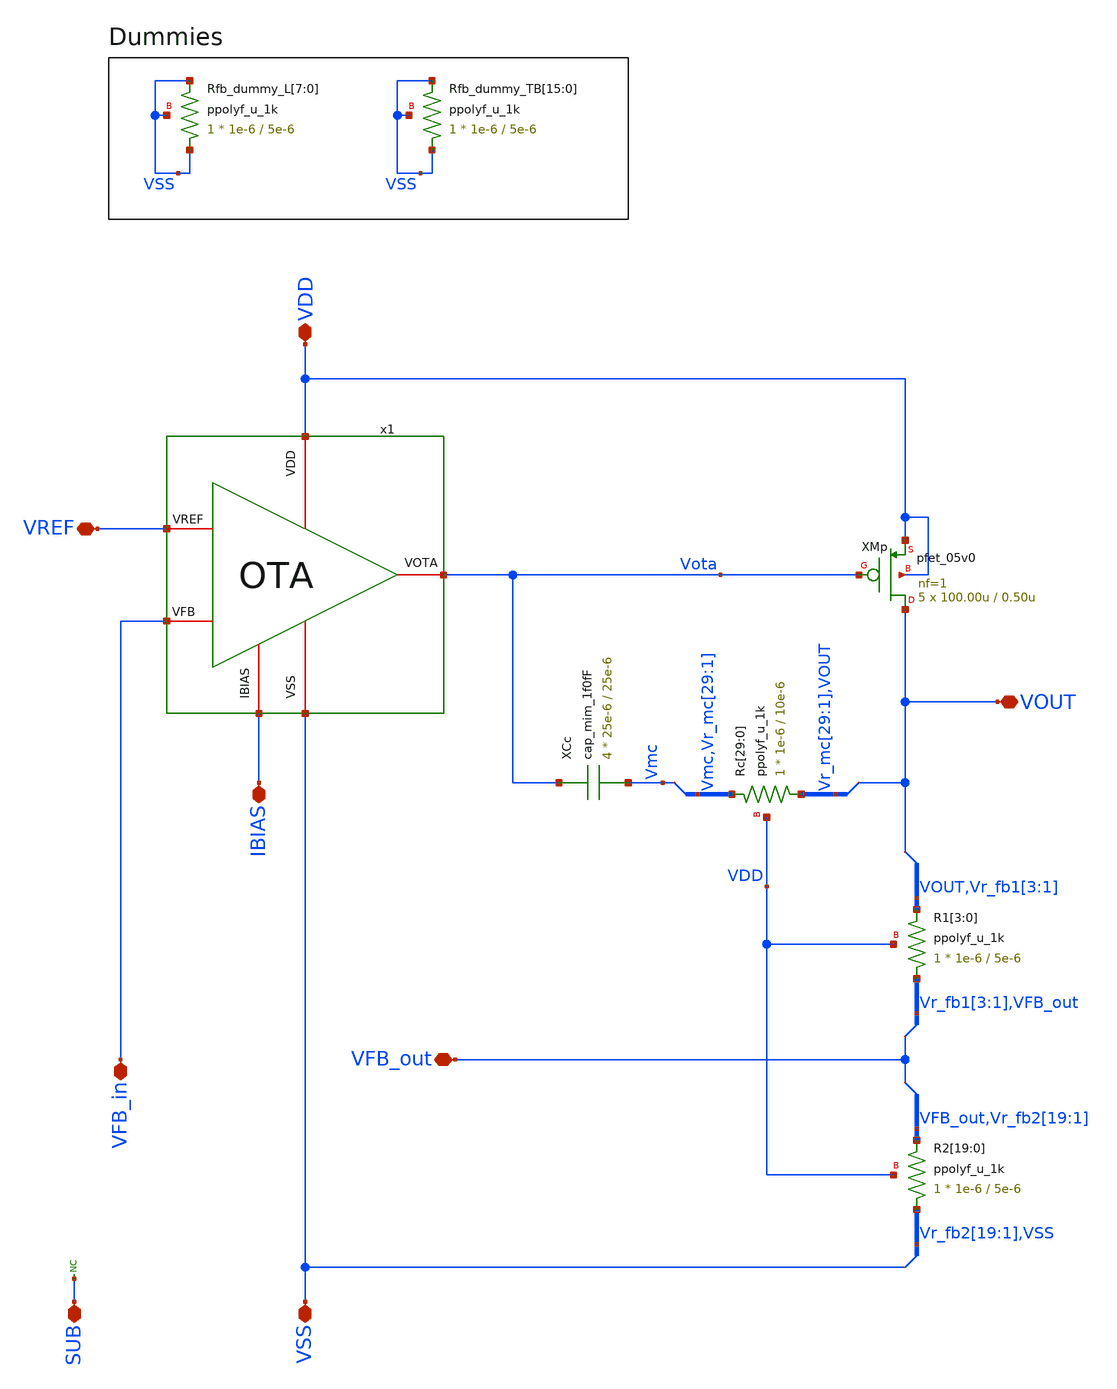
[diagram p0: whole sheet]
** sch_path: designs/libs/core_ldo/ldo/ldo_ldo_OL/ldo_OL.sch
**.subckt ldo_OL VFB_out VDD VSS VOUT SUB VREF IBIAS VFB_in
*.iopin VFB_out
*.iopin VDD
*.iopin VSS
*.iopin VOUT
*.iopin SUB
*.iopin VREF
*.iopin IBIAS
*.iopin VFB_in
XMp VOUT Vota VDD VDD pfet_05v0 L=0.50u W=100.00u nf=1 ad='int((nf+1)/2) * W/nf * 0.18u' as='int((nf+2)/2) * W/nf * 0.18u'
+ pd='2*int((nf+1)/2) * (W/nf + 0.18u)' ps='2*int((nf+2)/2) * (W/nf + 0.18u)' nrd='0.18u / W' nrs='0.18u / W'
+ sa=0 sb=0 sd=0 m=5
* noconn SUB
x1 VDD VREF VFB_in Vota IBIAS VSS OTA
XR1[3] Vr_fb1[3] VOUT VDD ppolyf_u_1k r_width=1e-6 r_length=5e-6 m=1
XR1[2] Vr_fb1[2] Vr_fb1[3] VDD ppolyf_u_1k r_width=1e-6 r_length=5e-6 m=1
XR1[1] Vr_fb1[1] Vr_fb1[2] VDD ppolyf_u_1k r_width=1e-6 r_length=5e-6 m=1
XR1[0] VFB_out Vr_fb1[1] VDD ppolyf_u_1k r_width=1e-6 r_length=5e-6 m=1
XR2[19] Vr_fb2[19] VFB_out VDD ppolyf_u_1k r_width=1e-6 r_length=5e-6 m=1
XR2[18] Vr_fb2[18] Vr_fb2[19] VDD ppolyf_u_1k r_width=1e-6 r_length=5e-6 m=1
XR2[17] Vr_fb2[17] Vr_fb2[18] VDD ppolyf_u_1k r_width=1e-6 r_length=5e-6 m=1
XR2[16] Vr_fb2[16] Vr_fb2[17] VDD ppolyf_u_1k r_width=1e-6 r_length=5e-6 m=1
XR2[15] Vr_fb2[15] Vr_fb2[16] VDD ppolyf_u_1k r_width=1e-6 r_length=5e-6 m=1
XR2[14] Vr_fb2[14] Vr_fb2[15] VDD ppolyf_u_1k r_width=1e-6 r_length=5e-6 m=1
XR2[13] Vr_fb2[13] Vr_fb2[14] VDD ppolyf_u_1k r_width=1e-6 r_length=5e-6 m=1
XR2[12] Vr_fb2[12] Vr_fb2[13] VDD ppolyf_u_1k r_width=1e-6 r_length=5e-6 m=1
XR2[11] Vr_fb2[11] Vr_fb2[12] VDD ppolyf_u_1k r_width=1e-6 r_length=5e-6 m=1
XR2[10] Vr_fb2[10] Vr_fb2[11] VDD ppolyf_u_1k r_width=1e-6 r_length=5e-6 m=1
XR2[9] Vr_fb2[9] Vr_fb2[10] VDD ppolyf_u_1k r_width=1e-6 r_length=5e-6 m=1
XR2[8] Vr_fb2[8] Vr_fb2[9] VDD ppolyf_u_1k r_width=1e-6 r_length=5e-6 m=1
XR2[7] Vr_fb2[7] Vr_fb2[8] VDD ppolyf_u_1k r_width=1e-6 r_length=5e-6 m=1
XR2[6] Vr_fb2[6] Vr_fb2[7] VDD ppolyf_u_1k r_width=1e-6 r_length=5e-6 m=1
XR2[5] Vr_fb2[5] Vr_fb2[6] VDD ppolyf_u_1k r_width=1e-6 r_length=5e-6 m=1
XR2[4] Vr_fb2[4] Vr_fb2[5] VDD ppolyf_u_1k r_width=1e-6 r_length=5e-6 m=1
XR2[3] Vr_fb2[3] Vr_fb2[4] VDD ppolyf_u_1k r_width=1e-6 r_length=5e-6 m=1
XR2[2] Vr_fb2[2] Vr_fb2[3] VDD ppolyf_u_1k r_width=1e-6 r_length=5e-6 m=1
XR2[1] Vr_fb2[1] Vr_fb2[2] VDD ppolyf_u_1k r_width=1e-6 r_length=5e-6 m=1
XR2[0] VSS Vr_fb2[1] VDD ppolyf_u_1k r_width=1e-6 r_length=5e-6 m=1
XRc[29] Vr_mc[29] Vmc VDD ppolyf_u_1k r_width=1e-6 r_length=10e-6 m=1
XRc[28] Vr_mc[28] Vr_mc[29] VDD ppolyf_u_1k r_width=1e-6 r_length=10e-6 m=1
XRc[27] Vr_mc[27] Vr_mc[28] VDD ppolyf_u_1k r_width=1e-6 r_length=10e-6 m=1
XRc[26] Vr_mc[26] Vr_mc[27] VDD ppolyf_u_1k r_width=1e-6 r_length=10e-6 m=1
XRc[25] Vr_mc[25] Vr_mc[26] VDD ppolyf_u_1k r_width=1e-6 r_length=10e-6 m=1
XRc[24] Vr_mc[24] Vr_mc[25] VDD ppolyf_u_1k r_width=1e-6 r_length=10e-6 m=1
XRc[23] Vr_mc[23] Vr_mc[24] VDD ppolyf_u_1k r_width=1e-6 r_length=10e-6 m=1
XRc[22] Vr_mc[22] Vr_mc[23] VDD ppolyf_u_1k r_width=1e-6 r_length=10e-6 m=1
XRc[21] Vr_mc[21] Vr_mc[22] VDD ppolyf_u_1k r_width=1e-6 r_length=10e-6 m=1
XRc[20] Vr_mc[20] Vr_mc[21] VDD ppolyf_u_1k r_width=1e-6 r_length=10e-6 m=1
XRc[19] Vr_mc[19] Vr_mc[20] VDD ppolyf_u_1k r_width=1e-6 r_length=10e-6 m=1
XRc[18] Vr_mc[18] Vr_mc[19] VDD ppolyf_u_1k r_width=1e-6 r_length=10e-6 m=1
XRc[17] Vr_mc[17] Vr_mc[18] VDD ppolyf_u_1k r_width=1e-6 r_length=10e-6 m=1
XRc[16] Vr_mc[16] Vr_mc[17] VDD ppolyf_u_1k r_width=1e-6 r_length=10e-6 m=1
XRc[15] Vr_mc[15] Vr_mc[16] VDD ppolyf_u_1k r_width=1e-6 r_length=10e-6 m=1
XRc[14] Vr_mc[14] Vr_mc[15] VDD ppolyf_u_1k r_width=1e-6 r_length=10e-6 m=1
XRc[13] Vr_mc[13] Vr_mc[14] VDD ppolyf_u_1k r_width=1e-6 r_length=10e-6 m=1
XRc[12] Vr_mc[12] Vr_mc[13] VDD ppolyf_u_1k r_width=1e-6 r_length=10e-6 m=1
XRc[11] Vr_mc[11] Vr_mc[12] VDD ppolyf_u_1k r_width=1e-6 r_length=10e-6 m=1
XRc[10] Vr_mc[10] Vr_mc[11] VDD ppolyf_u_1k r_width=1e-6 r_length=10e-6 m=1
XRc[9] Vr_mc[9] Vr_mc[10] VDD ppolyf_u_1k r_width=1e-6 r_length=10e-6 m=1
XRc[8] Vr_mc[8] Vr_mc[9] VDD ppolyf_u_1k r_width=1e-6 r_length=10e-6 m=1
XRc[7] Vr_mc[7] Vr_mc[8] VDD ppolyf_u_1k r_width=1e-6 r_length=10e-6 m=1
XRc[6] Vr_mc[6] Vr_mc[7] VDD ppolyf_u_1k r_width=1e-6 r_length=10e-6 m=1
XRc[5] Vr_mc[5] Vr_mc[6] VDD ppolyf_u_1k r_width=1e-6 r_length=10e-6 m=1
XRc[4] Vr_mc[4] Vr_mc[5] VDD ppolyf_u_1k r_width=1e-6 r_length=10e-6 m=1
XRc[3] Vr_mc[3] Vr_mc[4] VDD ppolyf_u_1k r_width=1e-6 r_length=10e-6 m=1
XRc[2] Vr_mc[2] Vr_mc[3] VDD ppolyf_u_1k r_width=1e-6 r_length=10e-6 m=1
XRc[1] Vr_mc[1] Vr_mc[2] VDD ppolyf_u_1k r_width=1e-6 r_length=10e-6 m=1
XRc[0] VOUT Vr_mc[1] VDD ppolyf_u_1k r_width=1e-6 r_length=10e-6 m=1
XCc Vota Vmc cap_mim_1f0fF c_width=25e-6 c_length=25e-6 m=4
XRfb_dummy_L[7] VSS VSS VSS ppolyf_u_1k r_width=1e-6 r_length=5e-6 m=1
XRfb_dummy_L[6] VSS VSS VSS ppolyf_u_1k r_width=1e-6 r_length=5e-6 m=1
XRfb_dummy_L[5] VSS VSS VSS ppolyf_u_1k r_width=1e-6 r_length=5e-6 m=1
XRfb_dummy_L[4] VSS VSS VSS ppolyf_u_1k r_width=1e-6 r_length=5e-6 m=1
XRfb_dummy_L[3] VSS VSS VSS ppolyf_u_1k r_width=1e-6 r_length=5e-6 m=1
XRfb_dummy_L[2] VSS VSS VSS ppolyf_u_1k r_width=1e-6 r_length=5e-6 m=1
XRfb_dummy_L[1] VSS VSS VSS ppolyf_u_1k r_width=1e-6 r_length=5e-6 m=1
XRfb_dummy_L[0] VSS VSS VSS ppolyf_u_1k r_width=1e-6 r_length=5e-6 m=1
XRfb_dummy_TB[15] VSS VSS VSS ppolyf_u_1k r_width=1e-6 r_length=5e-6 m=1
XRfb_dummy_TB[14] VSS VSS VSS ppolyf_u_1k r_width=1e-6 r_length=5e-6 m=1
XRfb_dummy_TB[13] VSS VSS VSS ppolyf_u_1k r_width=1e-6 r_length=5e-6 m=1
XRfb_dummy_TB[12] VSS VSS VSS ppolyf_u_1k r_width=1e-6 r_length=5e-6 m=1
XRfb_dummy_TB[11] VSS VSS VSS ppolyf_u_1k r_width=1e-6 r_length=5e-6 m=1
XRfb_dummy_TB[10] VSS VSS VSS ppolyf_u_1k r_width=1e-6 r_length=5e-6 m=1
XRfb_dummy_TB[9] VSS VSS VSS ppolyf_u_1k r_width=1e-6 r_length=5e-6 m=1
XRfb_dummy_TB[8] VSS VSS VSS ppolyf_u_1k r_width=1e-6 r_length=5e-6 m=1
XRfb_dummy_TB[7] VSS VSS VSS ppolyf_u_1k r_width=1e-6 r_length=5e-6 m=1
XRfb_dummy_TB[6] VSS VSS VSS ppolyf_u_1k r_width=1e-6 r_length=5e-6 m=1
XRfb_dummy_TB[5] VSS VSS VSS ppolyf_u_1k r_width=1e-6 r_length=5e-6 m=1
XRfb_dummy_TB[4] VSS VSS VSS ppolyf_u_1k r_width=1e-6 r_length=5e-6 m=1
XRfb_dummy_TB[3] VSS VSS VSS ppolyf_u_1k r_width=1e-6 r_length=5e-6 m=1
XRfb_dummy_TB[2] VSS VSS VSS ppolyf_u_1k r_width=1e-6 r_length=5e-6 m=1
XRfb_dummy_TB[1] VSS VSS VSS ppolyf_u_1k r_width=1e-6 r_length=5e-6 m=1
XRfb_dummy_TB[0] VSS VSS VSS ppolyf_u_1k r_width=1e-6 r_length=5e-6 m=1
**.ends

* expanding   symbol:  libs/core_ldo/ldo/ldo_OTA/OTA.sym # of pins=6
** sym_path: designs/libs/core_ldo/ldo/OTA.sym
** sch_path: designs/libs/core_ldo/ldo/OTA.sch
.subckt OTA VDD VREF VFB VOTA IBIAS VSS
*.iopin VDD
*.iopin VSS
*.iopin VOTA
*.iopin VREF
*.iopin IBIAS
*.iopin VFB
XM3 net2 net2 VDD VDD pfet_05v0 L=2.00u W=8.00u nf=1 ad='int((nf+1)/2) * W/nf * 0.18u' as='int((nf+2)/2) * W/nf * 0.18u'
+ pd='2*int((nf+1)/2) * (W/nf + 0.18u)' ps='2*int((nf+2)/2) * (W/nf + 0.18u)' nrd='0.18u / W' nrs='0.18u / W'
+ sa=0 sb=0 sd=0 m=1
XM4 net3 net3 VDD VDD pfet_05v0 L=2.00u W=8.00u nf=1 ad='int((nf+1)/2) * W/nf * 0.18u' as='int((nf+2)/2) * W/nf * 0.18u'
+ pd='2*int((nf+1)/2) * (W/nf + 0.18u)' ps='2*int((nf+2)/2) * (W/nf + 0.18u)' nrd='0.18u / W' nrs='0.18u / W'
+ sa=0 sb=0 sd=0 m=1
XM5 net4 net2 VDD VDD pfet_05v0 L=2.00u W=8.00u nf=1 ad='int((nf+1)/2) * W/nf * 0.18u' as='int((nf+2)/2) * W/nf * 0.18u'
+ pd='2*int((nf+1)/2) * (W/nf + 0.18u)' ps='2*int((nf+2)/2) * (W/nf + 0.18u)' nrd='0.18u / W' nrs='0.18u / W'
+ sa=0 sb=0 sd=0 m=1
XM6 VOTA net3 VDD VDD pfet_05v0 L=2.00u W=8.00u nf=1 ad='int((nf+1)/2) * W/nf * 0.18u' as='int((nf+2)/2) * W/nf * 0.18u'
+ pd='2*int((nf+1)/2) * (W/nf + 0.18u)' ps='2*int((nf+2)/2) * (W/nf + 0.18u)' nrd='0.18u / W' nrs='0.18u / W'
+ sa=0 sb=0 sd=0 m=2
XM9 IBIAS IBIAS VSS VSS nfet_05v0 L=2.00u W=4.00u nf=1 ad='int((nf+1)/2) * W/nf * 0.18u' as='int((nf+2)/2) * W/nf * 0.18u'
+ pd='2*int((nf+1)/2) * (W/nf + 0.18u)' ps='2*int((nf+2)/2) * (W/nf + 0.18u)' nrd='0.18u / W' nrs='0.18u / W'
+ sa=0 sb=0 sd=0 m=1
XM10 net1 IBIAS VSS VSS nfet_05v0 L=2.00u W=4.00u nf=1 ad='int((nf+1)/2) * W/nf * 0.18u' as='int((nf+2)/2) * W/nf * 0.18u'
+ pd='2*int((nf+1)/2) * (W/nf + 0.18u)' ps='2*int((nf+2)/2) * (W/nf + 0.18u)' nrd='0.18u / W' nrs='0.18u / W'
+ sa=0 sb=0 sd=0 m=1
XM7 net4 net4 VSS VSS nfet_05v0 L=2.00u W=4.00u nf=1 ad='int((nf+1)/2) * W/nf * 0.18u' as='int((nf+2)/2) * W/nf * 0.18u'
+ pd='2*int((nf+1)/2) * (W/nf + 0.18u)' ps='2*int((nf+2)/2) * (W/nf + 0.18u)' nrd='0.18u / W' nrs='0.18u / W'
+ sa=0 sb=0 sd=0 m=1
XM8 VOTA net4 VSS VSS nfet_05v0 L=2.00u W=4.00u nf=1 ad='int((nf+1)/2) * W/nf * 0.18u' as='int((nf+2)/2) * W/nf * 0.18u'
+ pd='2*int((nf+1)/2) * (W/nf + 0.18u)' ps='2*int((nf+2)/2) * (W/nf + 0.18u)' nrd='0.18u / W' nrs='0.18u / W'
+ sa=0 sb=0 sd=0 m=2
XM1 net2 VREF net1 net1 nfet_05v0 L=0.60u W=40.00u nf=1 ad='int((nf+1)/2) * W/nf * 0.18u' as='int((nf+2)/2) * W/nf * 0.18u'
+ pd='2*int((nf+1)/2) * (W/nf + 0.18u)' ps='2*int((nf+2)/2) * (W/nf + 0.18u)' nrd='0.18u / W' nrs='0.18u / W'
+ sa=0 sb=0 sd=0 m=1
XM2 net3 VFB net1 net1 nfet_05v0 L=0.60u W=40.00u nf=1 ad='int((nf+1)/2) * W/nf * 0.18u' as='int((nf+2)/2) * W/nf * 0.18u'
+ pd='2*int((nf+1)/2) * (W/nf + 0.18u)' ps='2*int((nf+2)/2) * (W/nf + 0.18u)' nrd='0.18u / W' nrs='0.18u / W'
+ sa=0 sb=0 sd=0 m=1
.ends

.end
